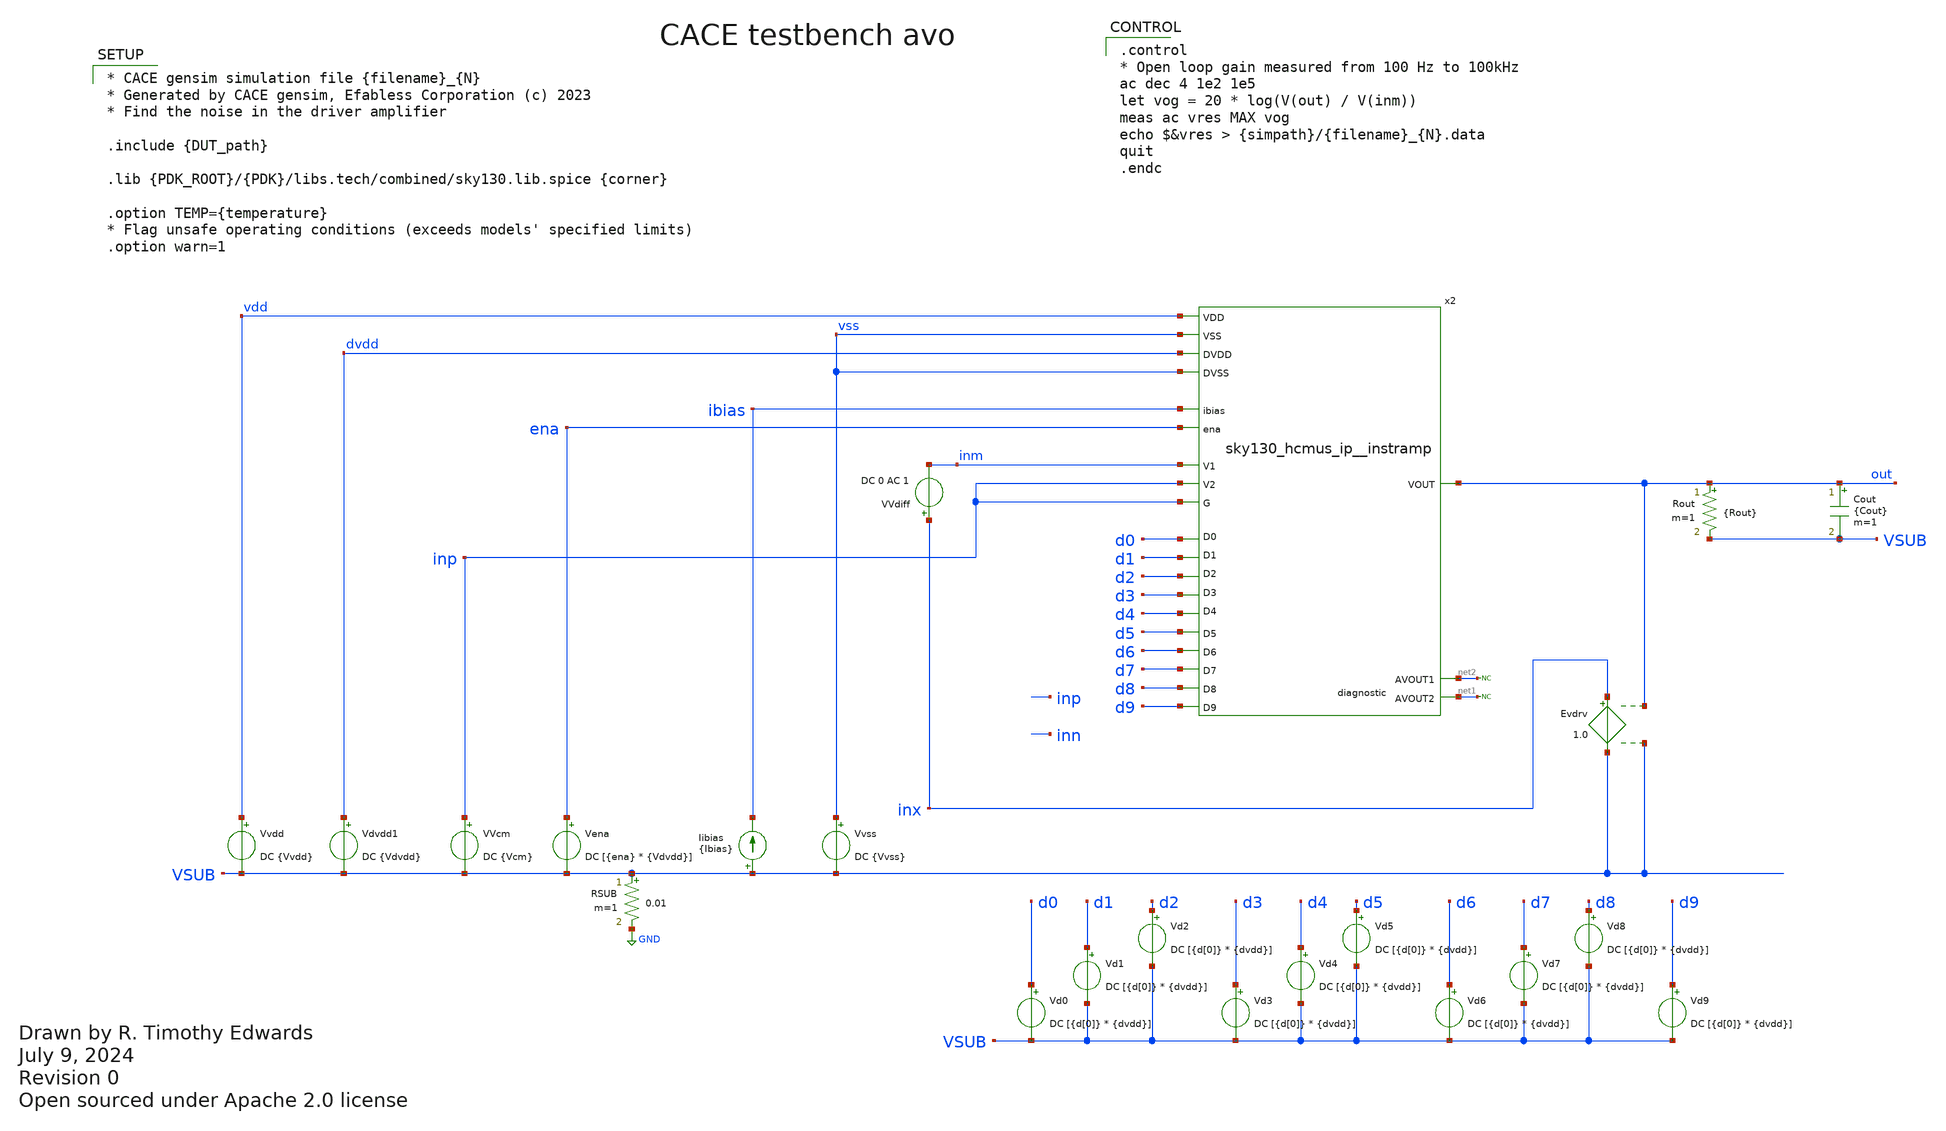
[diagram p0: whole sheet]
** sch_path: cace/templates/avo.sch
* Open sourced under Apache 2.0 license
**.subckt avo
VVcm inp VSUB DC {Vcm}
Vena ena VSUB DC [{ena} * {Vdvdd}]
Vvss vss VSUB DC {Vvss}
Rout out VSUB {Rout} m=1
Cout out VSUB {Cout} m=1
Vvdd vdd VSUB DC {Vvdd}
RSUB VSUB GND 0.01 m=1
Evdrv inx VSUB out VSUB 1.0
VVdiff inx inm DC 0 AC 1
x2 vdd vss inp inm inp d0 d1 d2 d3 d4 d5 d6 d7 d8 d9 net2 net1 out ibias ena dvdd vss
+ sky130_hcmus_ip__instramp
* noconn #net2
* noconn #net1
Vdvdd1 dvdd VSUB DC {Vdvdd}
Iibias VSUB ibias {Ibias}
Vd0 d0 VSUB DC [{d[0]} * {dvdd}]
Vd1 d1 VSUB DC [{d[0]} * {dvdd}]
Vd2 d2 VSUB DC [{d[0]} * {dvdd}]
Vd3 d3 VSUB DC [{d[0]} * {dvdd}]
Vd4 d4 VSUB DC [{d[0]} * {dvdd}]
Vd5 d5 VSUB DC [{d[0]} * {dvdd}]
Vd6 d6 VSUB DC [{d[0]} * {dvdd}]
Vd7 d7 VSUB DC [{d[0]} * {dvdd}]
Vd8 d8 VSUB DC [{d[0]} * {dvdd}]
Vd9 d9 VSUB DC [{d[0]} * {dvdd}]
**** begin user architecture code

.control
* Open loop gain measured from 100 Hz to 100kHz
ac dec 4 1e2 1e5
let vog = 20 * log(V(out) / V(inm))
meas ac vres MAX vog
echo $&vres > {simpath}/{filename}_{N}.data
quit
.endc



* CACE gensim simulation file {filename}_{N}
* Generated by CACE gensim, Efabless Corporation (c) 2023
* Find the noise in the driver amplifier

.include {DUT_path}

.lib {PDK_ROOT}/{PDK}/libs.tech/combined/sky130.lib.spice {corner}

.option TEMP={temperature}
* Flag unsafe operating conditions (exceeds models' specified limits)
.option warn=1


**** end user architecture code
**.ends
.GLOBAL GND
.end
